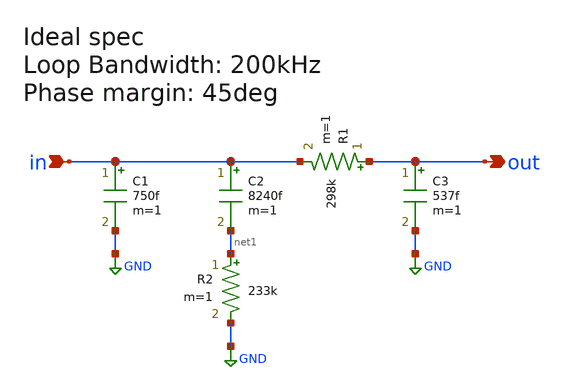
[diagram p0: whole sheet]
** sch_path: lf2.sch
**.subckt lf2 in out
*.ipin in
*.opin out
R2 net1 GND 233k m=1
C1 in GND 750f m=1
C2 in net1 8240f m=1
R1 out in 298k m=1
C3 out GND 537f m=1
**.ends
.GLOBAL GND
.end
